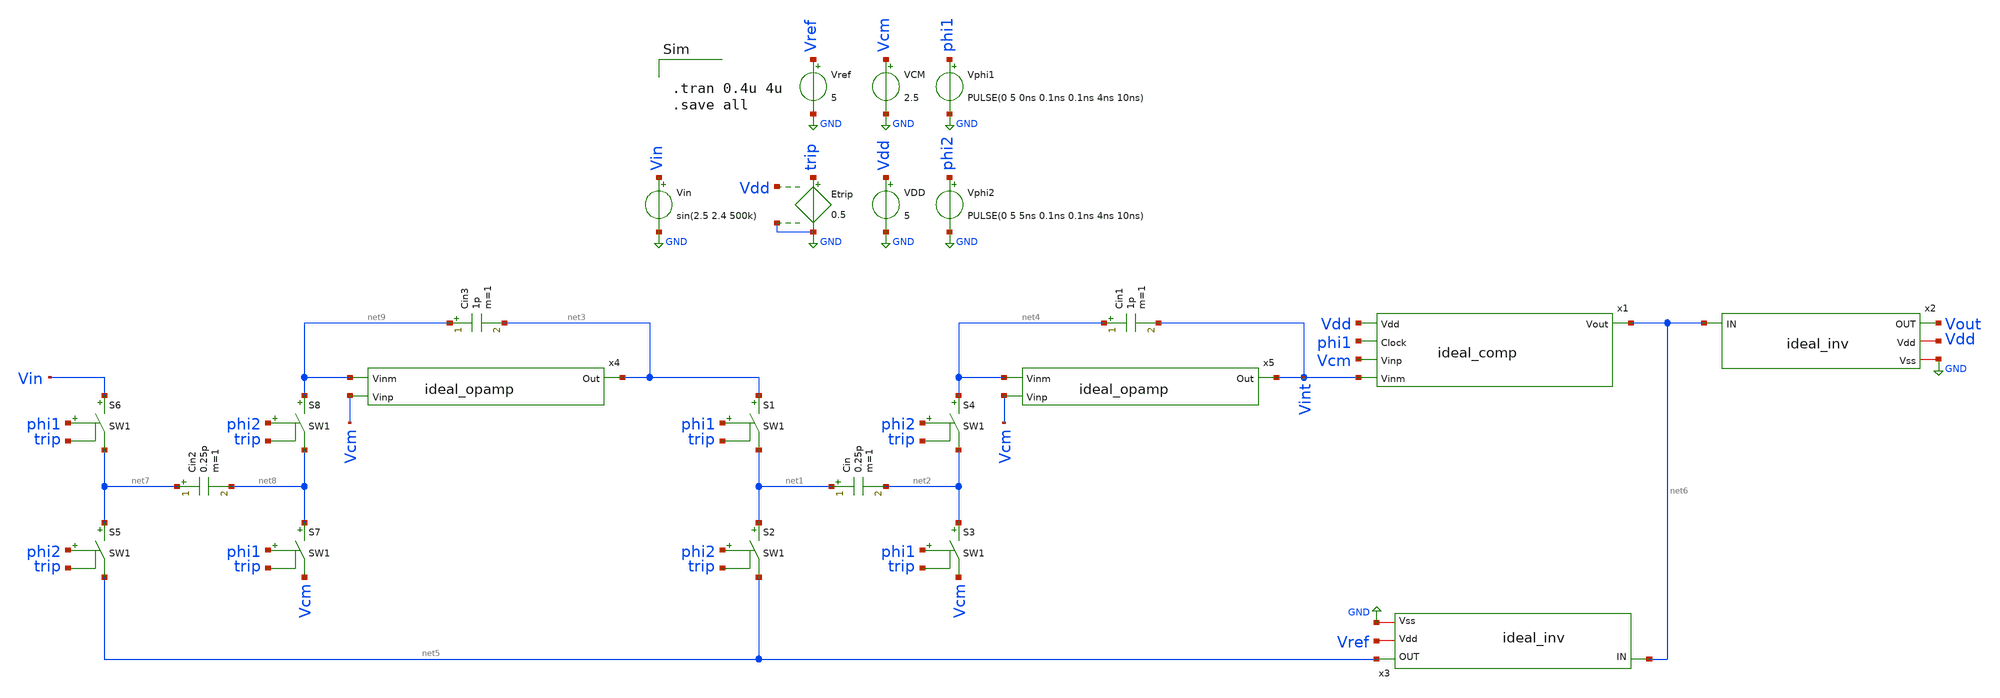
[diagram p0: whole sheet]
** sch_path: ideal_circuit/xschem/ideal_circuit_extended.sch
**.subckt ideal_circuit_extended
Etrip trip GND Vdd GND 0.5
Vref Vref GND 5
VDD Vdd GND 5
VCM Vcm GND 2.5
Vin Vin GND sin(2.5 2.4 500k)
Vphi1 phi1 GND PULSE(0 5 0ns 0.1ns 0.1ns 4ns 10ns)
Vphi2 phi2 GND PULSE(0 5 5ns 0.1ns 0.1ns 4ns 10ns)
Cin net1 net2 0.25p m=1
S2 net1 net5 phi2 trip SW1
S1 net3 net1 phi1 trip SW1
S3 net2 Vcm phi1 trip SW1
S4 net4 net2 phi2 trip SW1
Cin1 net4 Vint 1p m=1
x5 Vint net4 Vcm ideal_opamp
x1 net6 Vdd phi1 Vcm Vint ideal_comp
x3 net5 Vref net6 GND ideal_inv
x2 Vout Vdd net6 GND ideal_inv
Cin2 net7 net8 0.25p m=1
S5 net7 net5 phi2 trip SW1
S6 Vin net7 phi1 trip SW1
S7 net8 Vcm phi1 trip SW1
S8 net9 net8 phi2 trip SW1
Cin3 net9 net3 1p m=1
x4 net3 net9 Vcm ideal_opamp
**** begin user architecture code


.tran 0.4u 4u
.save all


**** end user architecture code
**.ends
.GLOBAL GND
**** begin user architecture code
.MODEL SW1 SW   VT=0.9 VH=0.01  RON=0.1 ROFF=10G
**** end user architecture code
.end
